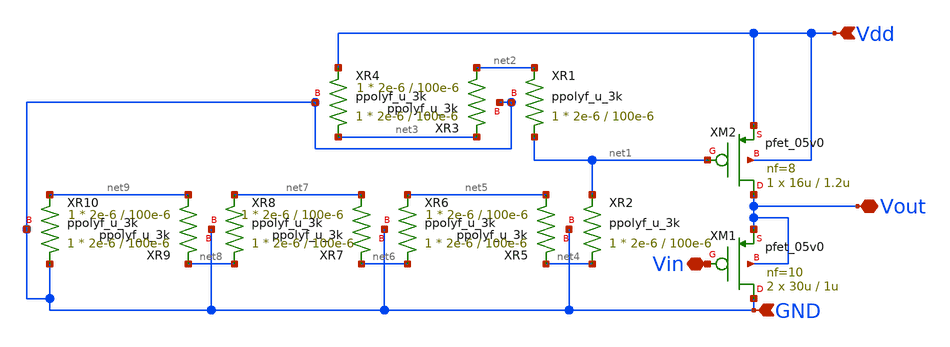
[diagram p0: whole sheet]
** sch_path: RN_buffer/buffer.sch
**.subckt buffer Vdd GND Vin Vout
*.ipin Vdd
*.ipin GND
*.iopin Vin
*.iopin Vout
XM1 GND Vin Vout Vout pfet_05v0 L=1u W=30u nf=10 ad='int((nf+1)/2) * W/nf * 0.18u' as='int((nf+2)/2) * W/nf * 0.18u'
+ pd='2*int((nf+1)/2) * (W/nf + 0.18u)' ps='2*int((nf+2)/2) * (W/nf + 0.18u)' nrd='0.18u / W' nrs='0.18u / W'
+ sa=0 sb=0 sd=0 m=2
XR1 net1 net2 GND ppolyf_u_3k r_width=2e-6 r_length=100e-6 m=1
XR2 net4 net1 GND ppolyf_u_3k r_width=2e-6 r_length=100e-6 m=1
XM2 Vout net1 Vdd Vdd pfet_05v0 L=1.2u W=16u nf=8 ad='int((nf+1)/2) * W/nf * 0.18u' as='int((nf+2)/2) * W/nf * 0.18u'
+ pd='2*int((nf+1)/2) * (W/nf + 0.18u)' ps='2*int((nf+2)/2) * (W/nf + 0.18u)' nrd='0.18u / W' nrs='0.18u / W'
+ sa=0 sb=0 sd=0 m=1
XR3 net2 net3 GND ppolyf_u_3k r_width=2e-6 r_length=100e-6 m=1
XR4 net3 Vdd GND ppolyf_u_3k r_width=2e-6 r_length=100e-6 m=1
XR5 net5 net4 GND ppolyf_u_3k r_width=2e-6 r_length=100e-6 m=1
XR6 net6 net5 GND ppolyf_u_3k r_width=2e-6 r_length=100e-6 m=1
XR7 net7 net6 GND ppolyf_u_3k r_width=2e-6 r_length=100e-6 m=1
XR8 net8 net7 GND ppolyf_u_3k r_width=2e-6 r_length=100e-6 m=1
XR9 net9 net8 GND ppolyf_u_3k r_width=2e-6 r_length=100e-6 m=1
XR10 GND net9 GND ppolyf_u_3k r_width=2e-6 r_length=100e-6 m=1
**.ends
.end
